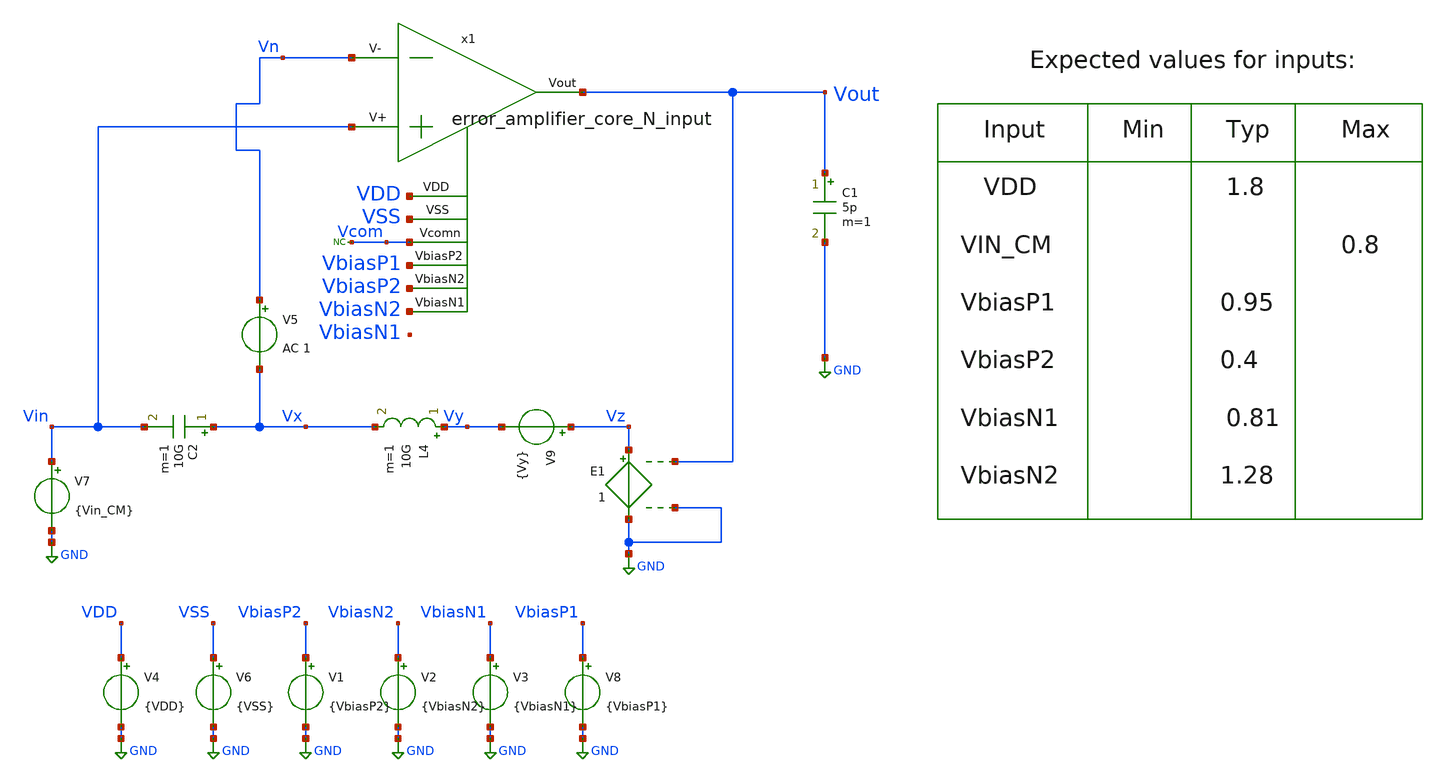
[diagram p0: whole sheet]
** sch_path: blocks/composite/folded_cascode/designs/gf180/error_amplifier_core_N_input/xschem/error_amplifier_core_Out_Swing_v2.sch
**.subckt error_amplifier_core_Out_Swing_v2
V5 Vn Vx AC 1
C2 Vx Vin 10G m=1
L4 Vy Vx 10G m=1
x1 VbiasP1 VbiasP2 VbiasN2 Vout Vin Vn VDD VSS Vcom error_amplifier_core_N_input
C1 Vout GND 5p m=1
* noconn Vcom
V1 VbiasP2 GND {VbiasP2}
V2 VbiasN2 GND {VbiasN2}
V3 VbiasN1 GND {VbiasN1}
V4 VDD GND {VDD}
V6 VSS GND {VSS}
V8 VbiasP1 GND {VbiasP1}
V7 Vin GND {Vin_CM}
V9 Vz Vy {Vy}
E1 Vz GND Vout GND 1
**** begin user architecture code




* --- Include PDK and Model Files ---
.include /foss/pdks/gf180mcuD/libs.tech/ngspice/design.ngspice
.lib /foss/pdks/gf180mcuD/libs.tech/ngspice/sm141064.ngspice typical

* --- Define Parameters for the Simulation ---
.param VDD = 1.8
.param VSS = 0
.param VbiasN1 = 0.81
.param VbiasN2 = 1.28
.param VbiasP1 = 0.95
.param VbiasP2 = 0.4
.param Vin_CM = 0.8
.param Vout_CM = 0.9
.param Vy = (Vout_CM - Vin_CM)
.param load_cap = 5*1e-12

* --- Simulation Commands and Analysis ---


*+ abstol=1e-14 savecurrents
.control
    save all

** OP simulation
op

** All OP parameters

let #####_M1_pmos_input_##### = 0
let id_M1 = @m.x1.xm1.m0[id]
let gm_M1 = @m.x1.xm1.m0[gm]
let ro_M1 = 1/@m.x1.xm1.m0[gds]
let Vsg_M1 = @m.x1.xm1.m0[vgs]
let Vsd_M1 = @m.x1.xm1.m0[vds]
let Vbs_M1 = -@m.x1.xm1.m0[vbs]
let Vdsat_M1 = @m.x1.xm1.m0[vdsat]
let Vth_M1 = @m.x1.xm1.m0[vth]
let ao_M1 = gm_M1*ro_M1
let gmid_M1 = gm_M1/id_M1
let fT_M1 = gm_M1/(6.283185*@m.x1.xm1.m0[cgg])
print #####_M1_pmos_input_##### id_M1 gm_M1 ro_M1 Vsg_M1 Vsd_M1 Vbs_M1 Vdsat_M1 Vth_M1 ao_M1 gmid_M1
+ fT_M1

let #####_M2_pmos_input_##### = 0
let id_M2 = @m.x1.xm2.m0[id]
let gm_M2 = @m.x1.xm2.m0[gm]
let ro_M2 = 1/@m.x1.xm2.m0[gds]
let Vsg_M2 = @m.x1.xm2.m0[vgs]
let Vsd_M2 = @m.x1.xm2.m0[vds]
let Vbs_M2 = -@m.x1.xm2.m0[vbs]
let Vdsat_M2 = @m.x1.xm2.m0[vdsat]
let Vth_M2 = @m.x1.xm2.m0[vth]
let ao_M2 = gm_M2*ro_M2
let gmid_M2 = gm_M2/id_M2
let fT_M2 = gm_M2/(6.283185*@m.x1.xm2.m0[cgg])
print #####_M2_pmos_input_##### id_M2 gm_M2 ro_M2 Vsg_M2 Vsd_M2 Vbs_M2 Vdsat_M2 Vth_M2 ao_M2 gmid_M2
+ fT_M2

let #####_M3_pmos_top_##### = 0
let id_M3 = @m.x1.xm3.m0[id]
let gm_M3 = @m.x1.xm3.m0[gm]
let ro_M3 = 1/@m.x1.xm3.m0[gds]
let Vsg_M3 = @m.x1.xm3.m0[vgs]
let Vsd_M3 = @m.x1.xm3.m0[vds]
let Vbs_M3 = -@m.x1.xm3.m0[vbs]
let Vdsat_M3 = @m.x1.xm3.m0[vdsat]
let Vth_M3 = @m.x1.xm3.m0[vth]
let ao_M3 = gm_M3*ro_M3
let gmid_M3 = gm_M3/id_M3
let fT_M3 = gm_M3/(6.283185*@m.x1.xm3.m0[cgg])
print #####_M3_pmos_top_##### id_M3 gm_M3 ro_M3 Vsg_M3 Vsd_M3 Vbs_M3 Vdsat_M3 Vth_M3 ao_M3 gmid_M3
+ fT_M3

let #####_M4_pmos_top_##### = 0
let id_M4 = @m.x1.xm4.m0[id]
let gm_M4 = @m.x1.xm4.m0[gm]
let ro_M4 = 1/@m.x1.xm4.m0[gds]
let Vsg_M4 = @m.x1.xm4.m0[vgs]
let Vsd_M4 = @m.x1.xm4.m0[vds]
let Vbs_M4 = -@m.x1.xm4.m0[vbs]
let Vdsat_M4 = @m.x1.xm4.m0[vdsat]
let Vth_M4 = @m.x1.xm4.m0[vth]
let ao_M4 = gm_M4*ro_M4
let gmid_M4 = gm_M4/id_M4
let fT_M4 = gm_M4/(6.283185*@m.x1.xm4.m0[cgg])
print #####_M4_pmos_top_##### id_M4 gm_M4 ro_M4 Vsg_M4 Vsd_M4 Vbs_M4 Vdsat_M4 Vth_M4 ao_M4 gmid_M4
+ fT_M4

let #####_M5_pmos_out_##### = 0
let id_M5 = @m.x1.xm5.m0[id]
let gm_M5 = @m.x1.xm5.m0[gm]
let ro_M5 = 1/@m.x1.xm5.m0[gds]
let Vsg_M5 = @m.x1.xm5.m0[vgs]
let Vsd_M5 = @m.x1.xm5.m0[vds]
let Vbs_M5 = -@m.x1.xm5.m0[vbs]
let Vdsat_M5 = @m.x1.xm5.m0[vdsat]
let Vth_M5 = @m.x1.xm5.m0[vth]
let ao_M5 = gm_M5*ro_M5
let gmid_M5 = gm_M5/id_M5
let fT_M5 = gm_M5/(6.283185*@m.x1.xm5.m0[cgg])
print #####_M5_pmos_out_##### id_M5 gm_M5 ro_M5 Vsg_M5 Vsd_M5 Vbs_M5 Vdsat_M5 Vth_M5 ao_M5 gmid_M5
+ fT_M5

let #####_M6_pmos_out_##### = 0
let id_M6 = @m.x1.xm6.m0[id]
let gm_M6 = @m.x1.xm6.m0[gm]
let ro_M6 = 1/@m.x1.xm6.m0[gds]
let Vsg_M6 = @m.x1.xm6.m0[vgs]
let Vsd_M6 = @m.x1.xm6.m0[vds]
let Vbs_M6 = -@m.x1.xm6.m0[vbs]
let Vdsat_M6 = @m.x1.xm6.m0[vdsat]
let Vth_M6 = @m.x1.xm6.m0[vth]
let ao_M6 = gm_M6*ro_M6
let gmid_M6 = gm_M6/id_M6
let fT_M6 = gm_M6/(6.283185*@m.x1.xm6.m0[cgg])
print #####_M6_pmos_out_##### id_M6 gm_M6 ro_M6 Vsg_M6 Vsd_M6 Vbs_M6 Vdsat_M6 Vth_M6 ao_M6 gmid_M6
+ fT_M6

let #####_M7_nmos_out_##### = 0
let id_M7 = @m.x1.xm7.m0[id]
let gm_M7 = @m.x1.xm7.m0[gm]
let ro_M7 = 1/@m.x1.xm7.m0[gds]
let Vgs_M7 = @m.x1.xm7.m0[vgs]
let Vds_M7 = @m.x1.xm7.m0[vds]
let Vsb_M7 = -@m.x1.xm7.m0[vbs]
let Vdsat_M7 = @m.x1.xm7.m0[vdsat]
let Vth_M7 = @m.x1.xm7.m0[vth]
let ao_M7 = gm_M7*ro_M7
let gmid_M7 = gm_M7/id_M7
let fT_M7 = gm_M7/(6.283185*@m.x1.xm7.m0[cgg])
print #####_M7_nmos_out_##### id_M7 gm_M7 ro_M7 Vgs_M7 Vds_M7 Vsb_M7 Vdsat_M7 Vth_M7 ao_M7 gmid_M7
+ fT_M7

let #####_M8_nmos_out_##### = 0
let id_M8 = @m.x1.xm8.m0[id]
let gm_M8 = @m.x1.xm8.m0[gm]
let ro_M8 = 1/@m.x1.xm8.m0[gds]
let Vgs_M8 = @m.x1.xm8.m0[vgs]
let Vds_M8 = @m.x1.xm8.m0[vds]
let Vsb_M8 = -@m.x1.xm8.m0[vbs]
let Vdsat_M8 = @m.x1.xm8.m0[vdsat]
let Vth_M8 = @m.x1.xm8.m0[vth]
let ao_M8 = gm_M8*ro_M8
let gmid_M8 = gm_M8/id_M8
let fT_M8 = gm_M8/(6.283185*@m.x1.xm8.m0[cgg])
print #####_M8_nmos_out_##### id_M8 gm_M8 ro_M8 Vgs_M8 Vds_M8 Vsb_M8 Vdsat_M8 Vth_M8 ao_M8 gmid_M8
+ fT_M8
let #####_M9_nmos_bottom_##### = 0
let id_M9 = @m.x1.xm9.m0[id]
let gm_M9 = @m.x1.xm9.m0[gm]
let ro_M9 = 1/@m.x1.xm9.m0[gds]
let Vgs_M9 = @m.x1.xm9.m0[vgs]
let Vds_M9 = @m.x1.xm9.m0[vds]
let Vsb_M9 = -@m.x1.xm9.m0[vbs]
let Vdsat_M9 = @m.x1.xm9.m0[vdsat]
let Vth_M9 = @m.x1.xm9.m0[vth]
let ao_M9 = gm_M9*ro_M9
let gmid_M9 = gm_M9/id_M9
let fT_M9 = gm_M9/(6.283185*@m.x1.xm9.m0[cgg])
print #####_M9_nmos_bottom_##### id_M9 gm_M9 ro_M9 Vgs_M9 Vds_M9 Vsb_M9 Vdsat_M9 Vth_M9 ao_M9
+ gmid_M9 fT_M9

let #####_M10_nmos_bottom_##### = 0
let id_M10 = @m.x1.xm10.m0[id]
let gm_M10 = @m.x1.xm10.m0[gm]
let ro_M10 = 1/@m.x1.xm10.m0[gds]
let Vgs_M10 = @m.x1.xm10.m0[vgs]
let Vds_M10 = @m.x1.xm10.m0[vds]
let Vsb_M10 = @m.x1.xm10.m0[vbs]
let Vdsat_M10 = @m.x1.xm10.m0[vdsat]
let Vth_M10 = @m.x1.xm10.m0[vth]
let ao_M10 = gm_M10*ro_M10
let gmid_M10 = gm_M10/id_M10
let fT_M10 = gm_M10/(6.283185*@m.x1.xm10.m0[cgg])
print #####_M10_nmos_bottom_##### id_M10 gm_M10 ro_M10 Vgs_M10 Vds_M10 Vsb_M10 Vdsat_M10 Vth_M10
+ ao_M10 gmid_M10 fT_M10

let #####_M11_pmos_mirror_##### = 0
let id_M11 = @m.x1.xm11.m0[id]
let gm_M11 = @m.x1.xm11.m0[gm]
let ro_M11 = 1/@m.x1.xm11.m0[gds]
let Vsg_M11 = @m.x1.xm11.m0[vgs]
let Vsd_M11 = @m.x1.xm11.m0[vds]
let Vbs_M11 = -@m.x1.xm11.m0[vbs]
let Vdsat_M11 = @m.x1.xm11.m0[vdsat]
let Vth_M11 = @m.x1.xm11.m0[vth]
let ao_M11 = gm_M11*ro_M11
let gmid_M11 = gm_M11/id_M11
let fT_M11 = gm_M11/(6.283185*@m.x1.xm11.m0[cgg])
print #####_M11_pmos_mirror_##### id_M11 gm_M11 ro_M11 Vsg_M11 Vsd_M11 Vbs_M11 Vdsat_M11 Vth_M11
+ ao_M11 gmid_M11 fT_M11

** Custom output
let #####_Custom_output_##### = 0

* DC_gain
let r1 = ao_M6*ro_M4
let r2 = ao_M8*((ro_M1*ro_M10)/(ro_M1+ro_M10))
let Rout = (r1*r2)/(r1+r2)
let Av = db(gm_M1*Rout)
* Bandwidth
let BW = 1/(Rout*1e-12*6.283185)
let BW_2 = 1/(Rout*5p*6.283185)


print #####_Custom_output_##### Av BW BW_2 Rout gm_M1 ro_M1 gm_M6 ro_M6 ro_M4 gm_M8 ro_M8 ro_M10


    remzerovec
    write error_amplifier_core_N_input_ac.raw
    set appendwrite

    * run ac simulation
    ac dec 20 1 100e7

    * measure parameters
    let vout_mag_VV = abs(v(Vout))
    let vout_mag = db(abs(v(Vout)))
    let vout_phase = cph(v(Vout)) * 180/pi
    let gm = (-1)*db(abs(v(Vout)))

    meas ac A0 find vout_mag at=1
    meas ac UGB when vout_mag=0 fall=1
    meas ac PM find vout_phase when vout_mag=0
    meas ac GM find gm when vout_phase=0

    let A0_p1 = A0 - 3
    meas ac BW when vout_mag=A0_p1

    *plot vout_mag
    *plot vout_phase

    write error_amplifier_core_N_input_ac.raw
.endc



**** end user architecture code
**.ends

* expanding   symbol:  gf180/error_amplifier_core_N_input/xschem/error_amplifier_core_N_input.sym #
*+ of pins=9
** sym_path: blocks/composite/folded_cascode/designs/gf180/error_amplifier_core_N_input/xschem/error_amplifier_core_N_input.sym
** sch_path: blocks/composite/folded_cascode/designs/gf180/error_amplifier_core_N_input/xschem/error_amplifier_core_N_input.sch
.subckt error_amplifier_core_N_input VbiasP2 VbiasN2 VbiasN1 Vout V+ V- VDD VSS Vcomn
*.ipin VbiasN2
*.iopin VDD
*.ipin VbiasP2
*.ipin VbiasN1
*.ipin V+
*.ipin V-
*.iopin VSS
*.iopin Vcomn
*.iopin Vout
XM4 Vdm6 Val VDD VDD pfet_03v3 L=0.3u W=4u nf=1 ad='int((nf+1)/2) * W/nf * 0.18u' as='int((nf+2)/2) * W/nf * 0.18u'
+ pd='2*int((nf+1)/2) * (W/nf + 0.18u)' ps='2*int((nf+2)/2) * (W/nf + 0.18u)' nrd='0.18u / W' nrs='0.18u / W'
+ sa=0 sb=0 sd=0 m=12
XM3 Vdm5 Val VDD VDD pfet_03v3 L=0.3u W=4u nf=1 ad='int((nf+1)/2) * W/nf * 0.18u' as='int((nf+2)/2) * W/nf * 0.18u'
+ pd='2*int((nf+1)/2) * (W/nf + 0.18u)' ps='2*int((nf+2)/2) * (W/nf + 0.18u)' nrd='0.18u / W' nrs='0.18u / W'
+ sa=0 sb=0 sd=0 m=12
XM5 Val VbiasP2 Vdm5 VDD pfet_03v3 L=2u W=6u nf=1 ad='int((nf+1)/2) * W/nf * 0.18u' as='int((nf+2)/2) * W/nf * 0.18u'
+ pd='2*int((nf+1)/2) * (W/nf + 0.18u)' ps='2*int((nf+2)/2) * (W/nf + 0.18u)' nrd='0.18u / W' nrs='0.18u / W'
+ sa=0 sb=0 sd=0 m=2
XM6 Vout VbiasP2 Vdm6 VDD pfet_03v3 L=2u W=6u nf=1 ad='int((nf+1)/2) * W/nf * 0.18u' as='int((nf+2)/2) * W/nf * 0.18u'
+ pd='2*int((nf+1)/2) * (W/nf + 0.18u)' ps='2*int((nf+2)/2) * (W/nf + 0.18u)' nrd='0.18u / W' nrs='0.18u / W'
+ sa=0 sb=0 sd=0 m=2
XM9 net1 VbiasN1 VSS VSS nfet_03v3 L=2u W=2u nf=1 ad='int((nf+1)/2) * W/nf * 0.18u' as='int((nf+2)/2) * W/nf * 0.18u'
+ pd='2*int((nf+1)/2) * (W/nf + 0.18u)' ps='2*int((nf+2)/2) * (W/nf + 0.18u)' nrd='0.18u / W' nrs='0.18u / W'
+ sa=0 sb=0 sd=0 m=2
XM8 Vout VbiasN2 Vcomn VSS nfet_03v3 L=2u W=5u nf=1 ad='int((nf+1)/2) * W/nf * 0.18u' as='int((nf+2)/2) * W/nf * 0.18u'
+ pd='2*int((nf+1)/2) * (W/nf + 0.18u)' ps='2*int((nf+2)/2) * (W/nf + 0.18u)' nrd='0.18u / W' nrs='0.18u / W'
+ sa=0 sb=0 sd=0 m=1
XM7 Val VbiasN2 net1 VSS nfet_03v3 L=2u W=5u nf=1 ad='int((nf+1)/2) * W/nf * 0.18u' as='int((nf+2)/2) * W/nf * 0.18u'
+ pd='2*int((nf+1)/2) * (W/nf + 0.18u)' ps='2*int((nf+2)/2) * (W/nf + 0.18u)' nrd='0.18u / W' nrs='0.18u / W'
+ sa=0 sb=0 sd=0 m=1
XM10 Vcomn VbiasN1 VSS VSS nfet_03v3 L=2u W=2u nf=1 ad='int((nf+1)/2) * W/nf * 0.18u' as='int((nf+2)/2) * W/nf * 0.18u'
+ pd='2*int((nf+1)/2) * (W/nf + 0.18u)' ps='2*int((nf+2)/2) * (W/nf + 0.18u)' nrd='0.18u / W' nrs='0.18u / W'
+ sa=0 sb=0 sd=0 m=2
XM15 VDD VDD VDD VDD pfet_03v3 L=3u W=1u nf=1 ad='int((nf+1)/2) * W/nf * 0.18u' as='int((nf+2)/2) * W/nf * 0.18u'
+ pd='2*int((nf+1)/2) * (W/nf + 0.18u)' ps='2*int((nf+2)/2) * (W/nf + 0.18u)' nrd='0.18u / W' nrs='0.18u / W'
+ sa=0 sb=0 sd=0 m=28
XM16 VDD VDD VDD VDD pfet_03v3 L=1.5u W=1u nf=1 ad='int((nf+1)/2) * W/nf * 0.18u' as='int((nf+2)/2) * W/nf * 0.18u'
+ pd='2*int((nf+1)/2) * (W/nf + 0.18u)' ps='2*int((nf+2)/2) * (W/nf + 0.18u)' nrd='0.18u / W' nrs='0.18u / W'
+ sa=0 sb=0 sd=0 m=20
XM13 VSS VSS VSS VSS nfet_03v3 L=3u W=1u nf=1 ad='int((nf+1)/2) * W/nf * 0.18u' as='int((nf+2)/2) * W/nf * 0.18u'
+ pd='2*int((nf+1)/2) * (W/nf + 0.18u)' ps='2*int((nf+2)/2) * (W/nf + 0.18u)' nrd='0.18u / W' nrs='0.18u / W'
+ sa=0 sb=0 sd=0 m=18
XM12 VSS VSS VSS VSS nfet_03v3 L=6.5u W=0.5u nf=1 ad='int((nf+1)/2) * W/nf * 0.18u' as='int((nf+2)/2) * W/nf * 0.18u'
+ pd='2*int((nf+1)/2) * (W/nf + 0.18u)' ps='2*int((nf+2)/2) * (W/nf + 0.18u)' nrd='0.18u / W' nrs='0.18u / W'
+ sa=0 sb=0 sd=0 m=36
XM14 VSS VSS VSS VSS nfet_03v3 L=1u W=1u nf=1 ad='int((nf+1)/2) * W/nf * 0.18u' as='int((nf+2)/2) * W/nf * 0.18u'
+ pd='2*int((nf+1)/2) * (W/nf + 0.18u)' ps='2*int((nf+2)/2) * (W/nf + 0.18u)' nrd='0.18u / W' nrs='0.18u / W'
+ sa=0 sb=0 sd=0 m=30
XM1 Vdm6 V- net2 VSS nfet_03v3 L=1u W=10u nf=1 ad='int((nf+1)/2) * W/nf * 0.18u' as='int((nf+2)/2) * W/nf * 0.18u'
+ pd='2*int((nf+1)/2) * (W/nf + 0.18u)' ps='2*int((nf+2)/2) * (W/nf + 0.18u)' nrd='0.18u / W' nrs='0.18u / W'
+ sa=0 sb=0 sd=0 m=20
XM2 Vdm5 V+ net2 VSS nfet_03v3 L=1u W=10u nf=1 ad='int((nf+1)/2) * W/nf * 0.18u' as='int((nf+2)/2) * W/nf * 0.18u'
+ pd='2*int((nf+1)/2) * (W/nf + 0.18u)' ps='2*int((nf+2)/2) * (W/nf + 0.18u)' nrd='0.18u / W' nrs='0.18u / W'
+ sa=0 sb=0 sd=0 m=20
XM11 net2 VbiasN1 VSS VSS nfet_03v3 L=2u W=2u nf=1 ad='int((nf+1)/2) * W/nf * 0.18u' as='int((nf+2)/2) * W/nf * 0.18u'
+ pd='2*int((nf+1)/2) * (W/nf + 0.18u)' ps='2*int((nf+2)/2) * (W/nf + 0.18u)' nrd='0.18u / W' nrs='0.18u / W'
+ sa=0 sb=0 sd=0 m=40
.ends

.GLOBAL GND
.end
